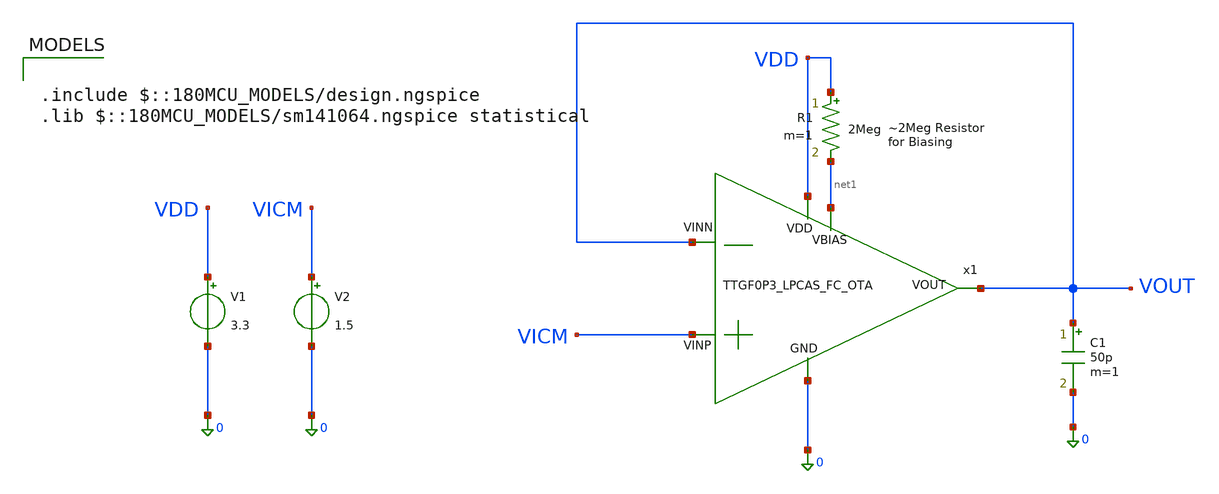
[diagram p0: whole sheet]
** sch_path: SCH/XSCHEM_SCH/tb_TTGF0P3_LPCAS_FC_OTA_MC.sch
**.subckt tb_TTGF0P3_LPCAS_FC_OTA_MC
x1 VDD net1 VOUT VICM VOUT 0 TTGF0P3_LPCAS_FC_OTA
V1 VDD 0 3.3
V2 VICM 0 1.5
R1 VDD net1 2Meg m=1
C1 VOUT 0 50p m=1
**** begin user architecture code

.include $::180MCU_MODELS/design.ngspice
.lib $::180MCU_MODELS/sm141064.ngspice statistical



.param sw_stat_global = 1
.param sw_stat_mismatch = 1
.option gmin=1e-18
.options savecurrents
.save all
.temp=27
.control
 let runs=1000
 let r=0
 dowhile r < runs
   reset
   let run=r
   op
   write /home/nithin/eda/LPCAS_TTSKY26a/tb_TTGF0P3_LPCAS_FC_OTA_MC.raw
   set appendwrite
   let DIFF_MIS=v(VICM)-v(Vout)
   print v(DIFF_MIS)
   wrdata /home/nithin/eda/ttgf0p3/tb_TTGF0P3_LPCAS_FC_OTA_MC.txt r v(DIFF_MIS)
   wrdata /home/nithin/eda/ttgf0p3/tb_TTGF0P3_LPCAS_FC_OTA_MC.csv r v(DIFF_MIS)

   let r = r + 1
 end
.endc

**** end user architecture code
**.ends

* expanding   symbol:  /home/nithin/eda/ttgf0p3/TTGF0P3_LPCAS_FC_OTA.sym # of pins=6
** sym_path: SCH/TTGF0P3_LPCAS_FC_OTA.sym
** sch_path: SCH/TTGF0P3_LPCAS_FC_OTA.sch
.subckt TTGF0P3_LPCAS_FC_OTA VDD VBIAS VOUT VINP VINN GND
*.opin VOUT
*.ipin VINP
*.ipin VINN
*.ipin VDD
*.ipin VBIAS
*.ipin GND
XM1 net11 VBIASCN net1 GND nfet_03v3 L=1u W=4u nf=1 ad='int((nf+1)/2) * W/nf * 0.18u' as='int((nf+2)/2) * W/nf * 0.18u'
+ pd='2*int((nf+1)/2) * (W/nf + 0.18u)' ps='2*int((nf+2)/2) * (W/nf + 0.18u)' nrd='0.18u / W' nrs='0.18u / W'
+ sa=0 sb=0 sd=0 m=1
XM2 VOUT VBIASCN net2 GND nfet_03v3 L=1u W=3u nf=1 ad='int((nf+1)/2) * W/nf * 0.18u' as='int((nf+2)/2) * W/nf * 0.18u'
+ pd='2*int((nf+1)/2) * (W/nf + 0.18u)' ps='2*int((nf+2)/2) * (W/nf + 0.18u)' nrd='0.18u / W' nrs='0.18u / W'
+ sa=0 sb=0 sd=0 m=1
XM5 net12 VBIASCP net4 VDD pfet_03v3 L=0.3u W=3u nf=1 ad='int((nf+1)/2) * W/nf * 0.18u' as='int((nf+2)/2) * W/nf * 0.18u'
+ pd='2*int((nf+1)/2) * (W/nf + 0.18u)' ps='2*int((nf+2)/2) * (W/nf + 0.18u)' nrd='0.18u / W' nrs='0.18u / W'
+ sa=0 sb=0 sd=0 m=1
XM6 net5 VBIASCP net3 VDD pfet_03v3 L=0.3u W=3u nf=1 ad='int((nf+1)/2) * W/nf * 0.18u' as='int((nf+2)/2) * W/nf * 0.18u'
+ pd='2*int((nf+1)/2) * (W/nf + 0.18u)' ps='2*int((nf+2)/2) * (W/nf + 0.18u)' nrd='0.18u / W' nrs='0.18u / W'
+ sa=0 sb=0 sd=0 m=1
XM7 net4 net5 net13 VDD pfet_03v3 L=1u W=8u nf=1 ad='int((nf+1)/2) * W/nf * 0.18u' as='int((nf+2)/2) * W/nf * 0.18u'
+ pd='2*int((nf+1)/2) * (W/nf + 0.18u)' ps='2*int((nf+2)/2) * (W/nf + 0.18u)' nrd='0.18u / W' nrs='0.18u / W'
+ sa=0 sb=0 sd=0 m=6
XM8 net3 net5 net14 VDD pfet_03v3 L=1u W=8u nf=1 ad='int((nf+1)/2) * W/nf * 0.18u' as='int((nf+2)/2) * W/nf * 0.18u'
+ pd='2*int((nf+1)/2) * (W/nf + 0.18u)' ps='2*int((nf+2)/2) * (W/nf + 0.18u)' nrd='0.18u / W' nrs='0.18u / W'
+ sa=0 sb=0 sd=0 m=6
XM9 VBIAS VBIAS GND GND nfet_03v3 L=3u W=2u nf=1 ad='int((nf+1)/2) * W/nf * 0.18u' as='int((nf+2)/2) * W/nf * 0.18u'
+ pd='2*int((nf+1)/2) * (W/nf + 0.18u)' ps='2*int((nf+2)/2) * (W/nf + 0.18u)' nrd='0.18u / W' nrs='0.18u / W'
+ sa=0 sb=0 sd=0 m=1
XM10 net9 VBIAS GND GND nfet_03v3 L=3u W=2u nf=1 ad='int((nf+1)/2) * W/nf * 0.18u' as='int((nf+2)/2) * W/nf * 0.18u'
+ pd='2*int((nf+1)/2) * (W/nf + 0.18u)' ps='2*int((nf+2)/2) * (W/nf + 0.18u)' nrd='0.18u / W' nrs='0.18u / W'
+ sa=0 sb=0 sd=0 m=5
XM3 net1 VBIAS GND GND nfet_03v3 L=3u W=2u nf=1 ad='int((nf+1)/2) * W/nf * 0.18u' as='int((nf+2)/2) * W/nf * 0.18u'
+ pd='2*int((nf+1)/2) * (W/nf + 0.18u)' ps='2*int((nf+2)/2) * (W/nf + 0.18u)' nrd='0.18u / W' nrs='0.18u / W'
+ sa=0 sb=0 sd=0 m=1
XM4 net2 VBIAS GND GND nfet_03v3 L=3u W=2u nf=1 ad='int((nf+1)/2) * W/nf * 0.18u' as='int((nf+2)/2) * W/nf * 0.18u'
+ pd='2*int((nf+1)/2) * (W/nf + 0.18u)' ps='2*int((nf+2)/2) * (W/nf + 0.18u)' nrd='0.18u / W' nrs='0.18u / W'
+ sa=0 sb=0 sd=0 m=1
XM14 net10 VBIAS GND GND nfet_03v3 L=3u W=2u nf=1 ad='int((nf+1)/2) * W/nf * 0.18u' as='int((nf+2)/2) * W/nf * 0.18u'
+ pd='2*int((nf+1)/2) * (W/nf + 0.18u)' ps='2*int((nf+2)/2) * (W/nf + 0.18u)' nrd='0.18u / W' nrs='0.18u / W'
+ sa=0 sb=0 sd=0 m=1
XM15 net15 VBIASCP VDD VDD pfet_03v3 L=0.3u W=0.3u nf=1 ad='int((nf+1)/2) * W/nf * 0.18u' as='int((nf+2)/2) * W/nf * 0.18u'
+ pd='2*int((nf+1)/2) * (W/nf + 0.18u)' ps='2*int((nf+2)/2) * (W/nf + 0.18u)' nrd='0.18u / W' nrs='0.18u / W'
+ sa=0 sb=0 sd=0 m=1
Vmeas net3 net7 0
.save i(vmeas)
Vmeas1 net4 net8 0
.save i(vmeas1)
Vmeas2 net6 net9 0
.save i(vmeas2)
Vmeas3 VBIASCP net10 0
.save i(vmeas3)
Vmeas4 net5 net11 0
.save i(vmeas4)
Vmeas5 net12 VOUT 0
.save i(vmeas5)
XM16 net7 VINP net6 GND nfet_03v3 L=1u W=8.5u nf=1 ad='int((nf+1)/2) * W/nf * 0.18u' as='int((nf+2)/2) * W/nf * 0.18u'
+ pd='2*int((nf+1)/2) * (W/nf + 0.18u)' ps='2*int((nf+2)/2) * (W/nf + 0.18u)' nrd='0.18u / W' nrs='0.18u / W'
+ sa=0 sb=0 sd=0 m=4
XM11 net8 VINN net6 GND nfet_03v3 L=1u W=8.5u nf=1 ad='int((nf+1)/2) * W/nf * 0.18u' as='int((nf+2)/2) * W/nf * 0.18u'
+ pd='2*int((nf+1)/2) * (W/nf + 0.18u)' ps='2*int((nf+2)/2) * (W/nf + 0.18u)' nrd='0.18u / W' nrs='0.18u / W'
+ sa=0 sb=0 sd=0 m=4
Vmeas6 VDD net14 0
.save i(vmeas6)
Vmeas7 VDD net13 0
.save i(vmeas7)
C1 VOUT GND 100p m=1
XM12 VBIASCP VBIASCP net15 VDD pfet_03v3 L=0.3u W=0.3u nf=1 ad='int((nf+1)/2) * W/nf * 0.18u' as='int((nf+2)/2) * W/nf * 0.18u'
+ pd='2*int((nf+1)/2) * (W/nf + 0.18u)' ps='2*int((nf+2)/2) * (W/nf + 0.18u)' nrd='0.18u / W' nrs='0.18u / W'
+ sa=0 sb=0 sd=0 m=1
XM17 net16 VBIASCP VDD VDD pfet_03v3 L=0.3u W=0.3u nf=1 ad='int((nf+1)/2) * W/nf * 0.18u' as='int((nf+2)/2) * W/nf * 0.18u'
+ pd='2*int((nf+1)/2) * (W/nf + 0.18u)' ps='2*int((nf+2)/2) * (W/nf + 0.18u)' nrd='0.18u / W' nrs='0.18u / W'
+ sa=0 sb=0 sd=0 m=1
XM18 VBIASCN VBIASCP net16 VDD pfet_03v3 L=0.3u W=0.3u nf=1 ad='int((nf+1)/2) * W/nf * 0.18u' as='int((nf+2)/2) * W/nf * 0.18u'
+ pd='2*int((nf+1)/2) * (W/nf + 0.18u)' ps='2*int((nf+2)/2) * (W/nf + 0.18u)' nrd='0.18u / W' nrs='0.18u / W'
+ sa=0 sb=0 sd=0 m=1
XM19 net17 VBIASCN GND GND nfet_03v3 L=1u W=1u nf=1 ad='int((nf+1)/2) * W/nf * 0.18u' as='int((nf+2)/2) * W/nf * 0.18u'
+ pd='2*int((nf+1)/2) * (W/nf + 0.18u)' ps='2*int((nf+2)/2) * (W/nf + 0.18u)' nrd='0.18u / W' nrs='0.18u / W'
+ sa=0 sb=0 sd=0 m=1
XM20 net18 VBIASCN net17 GND nfet_03v3 L=1u W=1u nf=1 ad='int((nf+1)/2) * W/nf * 0.18u' as='int((nf+2)/2) * W/nf * 0.18u'
+ pd='2*int((nf+1)/2) * (W/nf + 0.18u)' ps='2*int((nf+2)/2) * (W/nf + 0.18u)' nrd='0.18u / W' nrs='0.18u / W'
+ sa=0 sb=0 sd=0 m=1
XM21 VBIASCN VBIASCN net18 GND nfet_03v3 L=1u W=1u nf=1 ad='int((nf+1)/2) * W/nf * 0.18u' as='int((nf+2)/2) * W/nf * 0.18u'
+ pd='2*int((nf+1)/2) * (W/nf + 0.18u)' ps='2*int((nf+2)/2) * (W/nf + 0.18u)' nrd='0.18u / W' nrs='0.18u / W'
+ sa=0 sb=0 sd=0 m=1
.ends

.end
